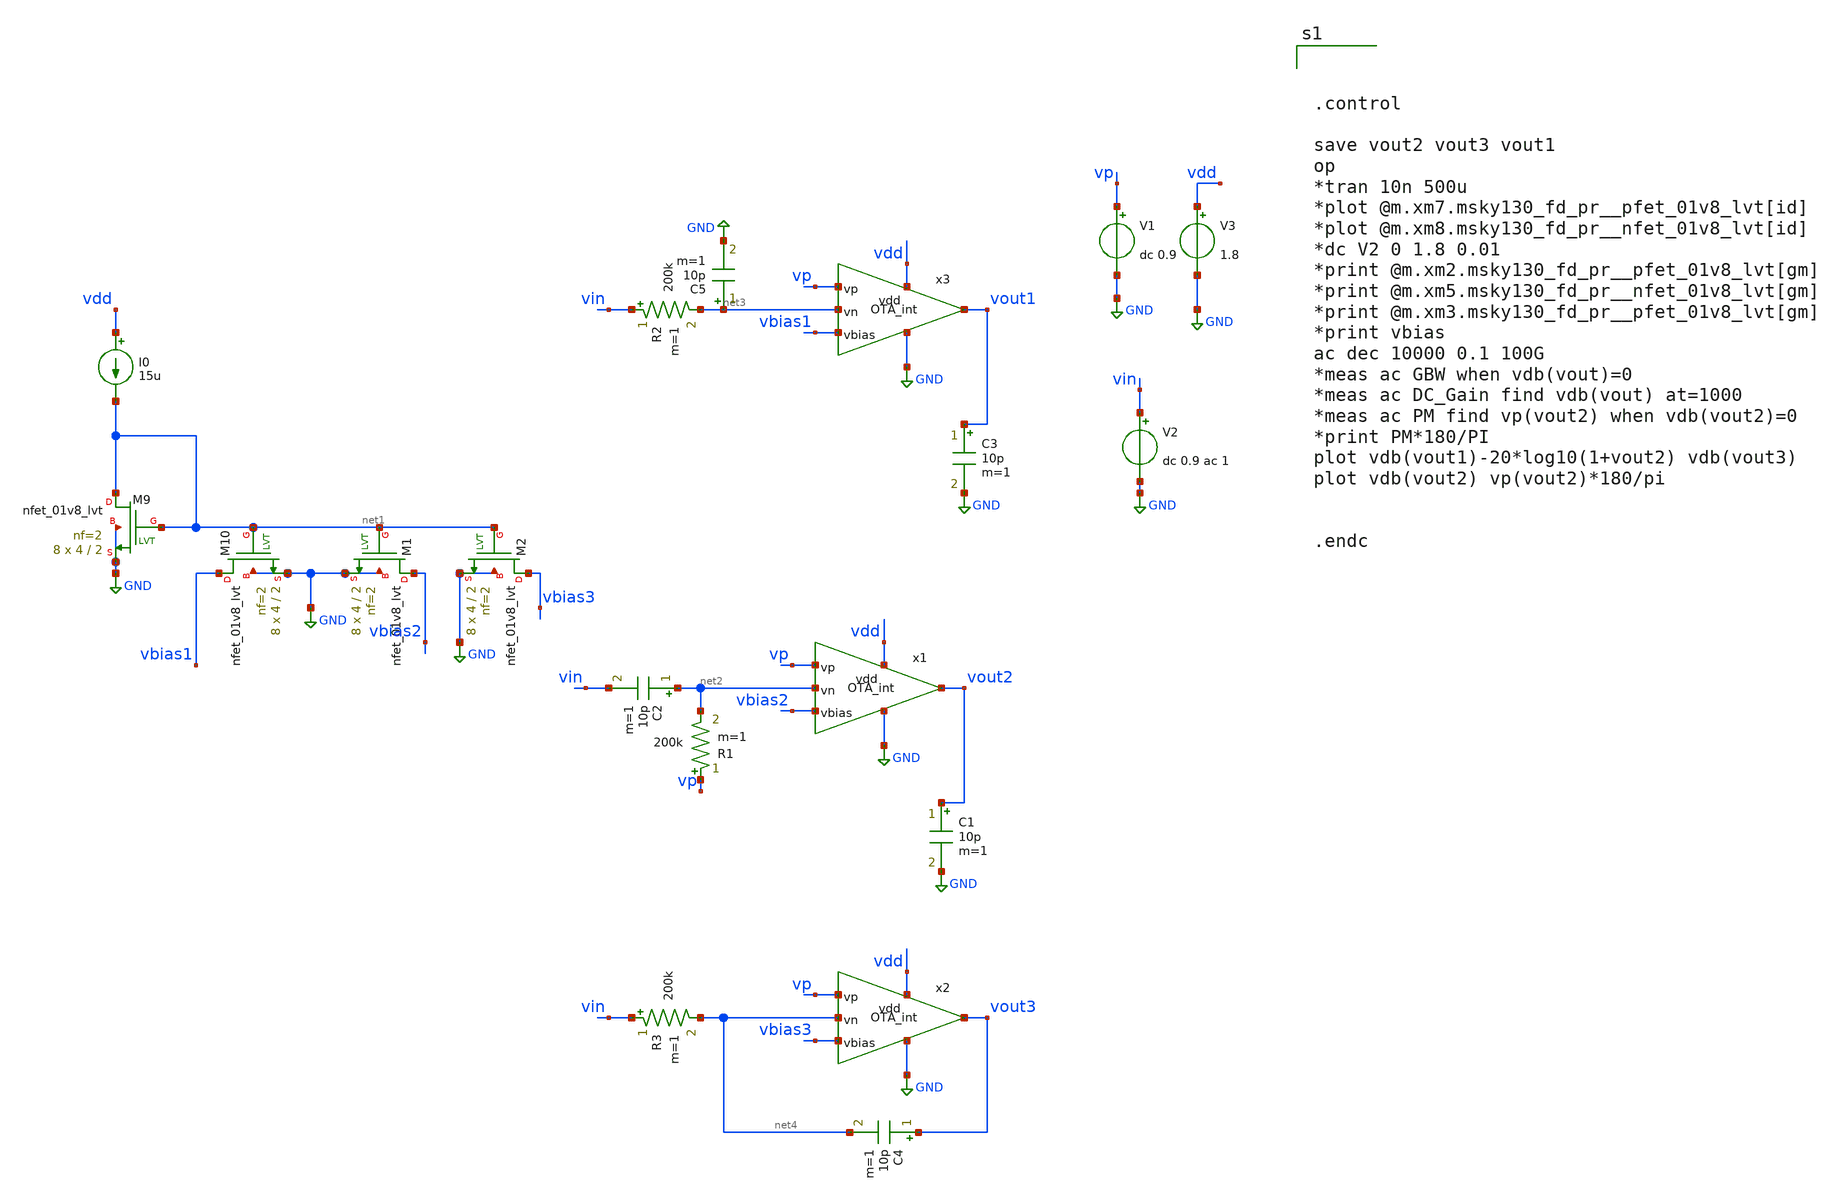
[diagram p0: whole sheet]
** sch_path: xschem/src/OTA_int/OTA_int_post_tb.sch
**.subckt OTA_int_post_tb
I0 vdd net1 15u
V1 vp GND dc 0.9
V3 vdd GND 1.8
XM9 net1 net1 GND GND sky130_fd_pr__nfet_01v8_lvt L=2 W=4 nf=2 ad='int((nf+1)/2) * W/nf * 0.29' as='int((nf+2)/2) * W/nf * 0.29'
+ pd='2*int((nf+1)/2) * (W/nf + 0.29)' ps='2*int((nf+2)/2) * (W/nf + 0.29)' nrd='0.29 / W' nrs='0.29 / W'
+ sa=0 sb=0 sd=0 mult=8 m=8
XM10 vbias1 net1 GND GND sky130_fd_pr__nfet_01v8_lvt L=2 W=4 nf=2 ad='int((nf+1)/2) * W/nf * 0.29' as='int((nf+2)/2) * W/nf * 0.29'
+ pd='2*int((nf+1)/2) * (W/nf + 0.29)' ps='2*int((nf+2)/2) * (W/nf + 0.29)' nrd='0.29 / W' nrs='0.29 / W'
+ sa=0 sb=0 sd=0 mult=8 m=8
R1 vp net2 200k m=1
C1 vout2 GND 10p m=1
C2 net2 vin 10p m=1
V2 vin GND dc 0.9 ac 1
R2 vin net3 200k m=1
C3 vout1 GND 10p m=1
C5 net3 GND 10p m=1
R3 vin net4 200k m=1
C4 vout3 net4 10p m=1
x3 vdd vp net3 vbias1 GND vout1 OTA_int
x1 vdd vp net2 vbias2 GND vout2 OTA_int
x2 vdd vp net4 vbias3 GND vout3 OTA_int
XM1 vbias2 net1 GND GND sky130_fd_pr__nfet_01v8_lvt L=2 W=4 nf=2 ad='int((nf+1)/2) * W/nf * 0.29' as='int((nf+2)/2) * W/nf * 0.29'
+ pd='2*int((nf+1)/2) * (W/nf + 0.29)' ps='2*int((nf+2)/2) * (W/nf + 0.29)' nrd='0.29 / W' nrs='0.29 / W'
+ sa=0 sb=0 sd=0 mult=8 m=8
XM2 vbias3 net1 GND GND sky130_fd_pr__nfet_01v8_lvt L=2 W=4 nf=2 ad='int((nf+1)/2) * W/nf * 0.29' as='int((nf+2)/2) * W/nf * 0.29'
+ pd='2*int((nf+1)/2) * (W/nf + 0.29)' ps='2*int((nf+2)/2) * (W/nf + 0.29)' nrd='0.29 / W' nrs='0.29 / W'
+ sa=0 sb=0 sd=0 mult=8 m=8
**** begin user architecture code



.control

save vout2 vout3 vout1
op
*tran 10n 500u
*plot @m.xm7.msky130_fd_pr__pfet_01v8_lvt[id]
*plot @m.xm8.msky130_fd_pr__nfet_01v8_lvt[id]
*dc V2 0 1.8 0.01
*print @m.xm2.msky130_fd_pr__pfet_01v8_lvt[gm]
*print @m.xm5.msky130_fd_pr__nfet_01v8_lvt[gm]
*print @m.xm3.msky130_fd_pr__pfet_01v8_lvt[gm]
*print vbias
ac dec 10000 0.1 100G
*meas ac GBW when vdb(vout)=0
*meas ac DC_Gain find vdb(vout) at=1000
*meas ac PM find vp(vout2) when vdb(vout2)=0
*print PM*180/PI
plot vdb(vout1)-20*log10(1+vout2) vdb(vout3)
plot vdb(vout2) vp(vout2)*180/pi


.endc



.include /home/eda/pdk/skywater-pdk/libraries/sky130_fd_pr_ngspice/latest/models/corners/tt.spice
.include /home/eda/magic/class_d_audio_amplifier/OTA/OTA_post.spice
.include /home/eda/magic/class_d_audio_amplifier/OTA/OTA_tri_post.spice
.include /home/eda/magic/class_d_audio_amplifier/OTA/OTA_int_post.spice
.include /home/eda/magic/class_d_audio_amplifier/OTA/OTA_int_revised_post.spice
* Resistor$::SKYWATER_MODELS/Capacitor
.include $::SKYWATER_MODELS/models/r+c/res_typical__cap_typical.spice
.include $::SKYWATER_MODELS/models/r+c/res_typical__cap_typical__lin.spice
* Special cells
.include $::SKYWATER_MODELS/models/corners/tt/specialized_cells.spice


**** end user architecture code
**.ends

* expanding   symbol:  src/OTA_int/OTA_int.sym # of pins=6
** sym_path: xschem/src/OTA_int/OTA_int.sym
** sch_path: xschem/src/OTA_int/OTA_int.sch
.subckt OTA_int vdd vp vn vbias vss vout
*.ipin vp
*.ipin vn
*.ipin vbias
*.iopin vss
*.iopin vdd
*.opin vout
XM1 v1 vp vc vc sky130_fd_pr__pfet_01v8_lvt L=1 W=4 nf=1 ad='int((nf+1)/2) * W/nf * 0.29' as='int((nf+2)/2) * W/nf * 0.29'
+ pd='2*int((nf+1)/2) * (W/nf + 0.29)' ps='2*int((nf+2)/2) * (W/nf + 0.29)' nrd='0.29 / W' nrs='0.29 / W'
+ sa=0 sb=0 sd=0 mult=16 m=16
XM2 vf vn vc vc sky130_fd_pr__pfet_01v8_lvt L=1 W=4 nf=1 ad='int((nf+1)/2) * W/nf * 0.29' as='int((nf+2)/2) * W/nf * 0.29'
+ pd='2*int((nf+1)/2) * (W/nf + 0.29)' ps='2*int((nf+2)/2) * (W/nf + 0.29)' nrd='0.29 / W' nrs='0.29 / W'
+ sa=0 sb=0 sd=0 mult=16 m=16
XM3 vc vbias vdd vdd sky130_fd_pr__pfet_01v8_lvt L=1 W=2 nf=2 ad='int((nf+1)/2) * W/nf * 0.29' as='int((nf+2)/2) * W/nf * 0.29'
+ pd='2*int((nf+1)/2) * (W/nf + 0.29)' ps='2*int((nf+2)/2) * (W/nf + 0.29)' nrd='0.29 / W' nrs='0.29 / W'
+ sa=0 sb=0 sd=0 mult=24 m=24
XM4 v1 vf vss vss sky130_fd_pr__nfet_01v8_lvt L=1 W=1 nf=1 ad='int((nf+1)/2) * W/nf * 0.29' as='int((nf+2)/2) * W/nf * 0.29'
+ pd='2*int((nf+1)/2) * (W/nf + 0.29)' ps='2*int((nf+2)/2) * (W/nf + 0.29)' nrd='0.29 / W' nrs='0.29 / W'
+ sa=0 sb=0 sd=0 mult=16 m=16
XM5 vf vf vss vss sky130_fd_pr__nfet_01v8_lvt L=1 W=1 nf=1 ad='int((nf+1)/2) * W/nf * 0.29' as='int((nf+2)/2) * W/nf * 0.29'
+ pd='2*int((nf+1)/2) * (W/nf + 0.29)' ps='2*int((nf+2)/2) * (W/nf + 0.29)' nrd='0.29 / W' nrs='0.29 / W'
+ sa=0 sb=0 sd=0 mult=16 m=16
XM6 vbias vbias vdd vdd sky130_fd_pr__pfet_01v8_lvt L=1 W=2 nf=2 ad='int((nf+1)/2) * W/nf * 0.29' as='int((nf+2)/2) * W/nf * 0.29'
+ pd='2*int((nf+1)/2) * (W/nf + 0.29)' ps='2*int((nf+2)/2) * (W/nf + 0.29)' nrd='0.29 / W' nrs='0.29 / W'
+ sa=0 sb=0 sd=0 mult=24 m=24
XM7 vout vbias vdd vdd sky130_fd_pr__pfet_01v8_lvt L=1 W=2 nf=2 ad='int((nf+1)/2) * W/nf * 0.29' as='int((nf+2)/2) * W/nf * 0.29'
+ pd='2*int((nf+1)/2) * (W/nf + 0.29)' ps='2*int((nf+2)/2) * (W/nf + 0.29)' nrd='0.29 / W' nrs='0.29 / W'
+ sa=0 sb=0 sd=0 mult=48 m=48
XM8 vout v1 vss vss sky130_fd_pr__nfet_01v8_lvt L=1 W=1 nf=1 ad='int((nf+1)/2) * W/nf * 0.29' as='int((nf+2)/2) * W/nf * 0.29'
+ pd='2*int((nf+1)/2) * (W/nf + 0.29)' ps='2*int((nf+2)/2) * (W/nf + 0.29)' nrd='0.29 / W' nrs='0.29 / W'
+ sa=0 sb=0 sd=0 mult=64 m=64
XC1 v2 vout sky130_fd_pr__cap_mim_m3_1 W=14 L=30 MF=1 m=1
XR1 v1 v2 vss sky130_fd_pr__res_xhigh_po L=2.8 mult=1 m=1
XC2 v2 vout sky130_fd_pr__cap_mim_m3_1 W=30 L=14 MF=1 m=1
.ends

.GLOBAL GND
.end
